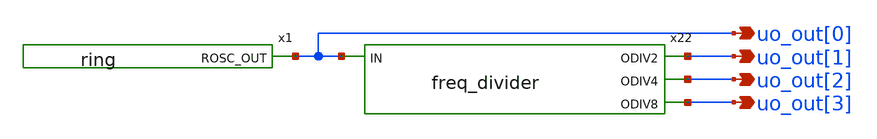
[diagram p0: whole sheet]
** sch_path: xschem/tt_um_oscillating_bones.sch
**.subckt tt_um_oscillating_bones uo_out[1] uo_out[0] uo_out[2] uo_out[3]
*.opin uo_out[1]
*.opin uo_out[0]
*.opin uo_out[2]
*.opin uo_out[3]
x22 uo_out[1] uo_out[2] uo_out[3] uo_out[0] freq_divider
x1 uo_out[0] ring
**.ends

* expanding   symbol:  freq_divider.sym # of pins=4
** sym_path: xschem/freq_divider.sym
** sch_path: xschem/freq_divider.sch
.subckt freq_divider ODIV2 ODIV4 ODIV8 IN
*.ipin IN
*.opin ODIV2
*.opin ODIV4
*.opin ODIV8
x1 IN net3 VGND VNB VPB VPWR ODIV2 net3 sky130_fd_sc_hd__dfxbp_1
x2 ODIV2 net1 VGND VNB VPB VPWR ODIV4 net1 sky130_fd_sc_hd__dfxbp_1
x3 ODIV4 net2 VGND VNB VPB VPWR ODIV8 net2 sky130_fd_sc_hd__dfxbp_1
.ends


* expanding   symbol:  ring.sym # of pins=1
** sym_path: xschem/ring.sym
** sch_path: xschem/ring.sch
.subckt ring ROSC_OUT
*.opin ROSC_OUT
x1 net20 net1 skullfet_inverter
x2 net1 net3 skullfet_inverter
x3 net3 net2 skullfet_inverter
x4 net2 ROSC_OUT skullfet_inverter
x5 ROSC_OUT net4 skullfet_inverter
x7 net5 net6 skullfet_inverter
x6 net4 net5 skullfet_inverter
x8 net6 net7 skullfet_inverter
x9 net7 net11 skullfet_inverter
x10 net11 net8 skullfet_inverter
x11 net8 net9 skullfet_inverter
x12 net9 net10 skullfet_inverter
x13 net10 net12 skullfet_inverter
x14 net12 net13 skullfet_inverter
x15 net13 net14 skullfet_inverter
x16 net14 net15 skullfet_inverter
x17 net15 net16 skullfet_inverter
x18 net16 net17 skullfet_inverter
x19 net17 net18 skullfet_inverter
x20 net18 net19 skullfet_inverter
x21 net19 net20 skullfet_inverter
.ends


* expanding   symbol:  skullfet_inverter.sym # of pins=2
** sym_path: xschem/skullfet_inverter.sym
** sch_path: xschem/skullfet_inverter.sch
.subckt skullfet_inverter A Y
*.ipin A
*.opin Y
XM1 Y A VPWR VPWR sky130_fd_pr__pfet_01v8_hvt L=0.4 W=4.05 nf=1 ad=6.2694 as=4.4307 pd=26.64 ps=10.9
+ nrd='0.29 / 4.05 ' nrs='0.29 / 4.05 ' sa=0 sb=0 sd=0 mult=1 m=1
XM2 Y A VGND VGND sky130_fd_pr__nfet_01v8 L=0.4 W=4.05 nf=1 ad=4.2687 as=6.4314 pd=10.82 ps=26.72 nrd='0.29 / 4.05 '
+ nrs='0.29 / 4.05 ' sa=0 sb=0 sd=0 mult=1 m=1
.ends

.GLOBAL VGND
.GLOBAL VPWR
.end
